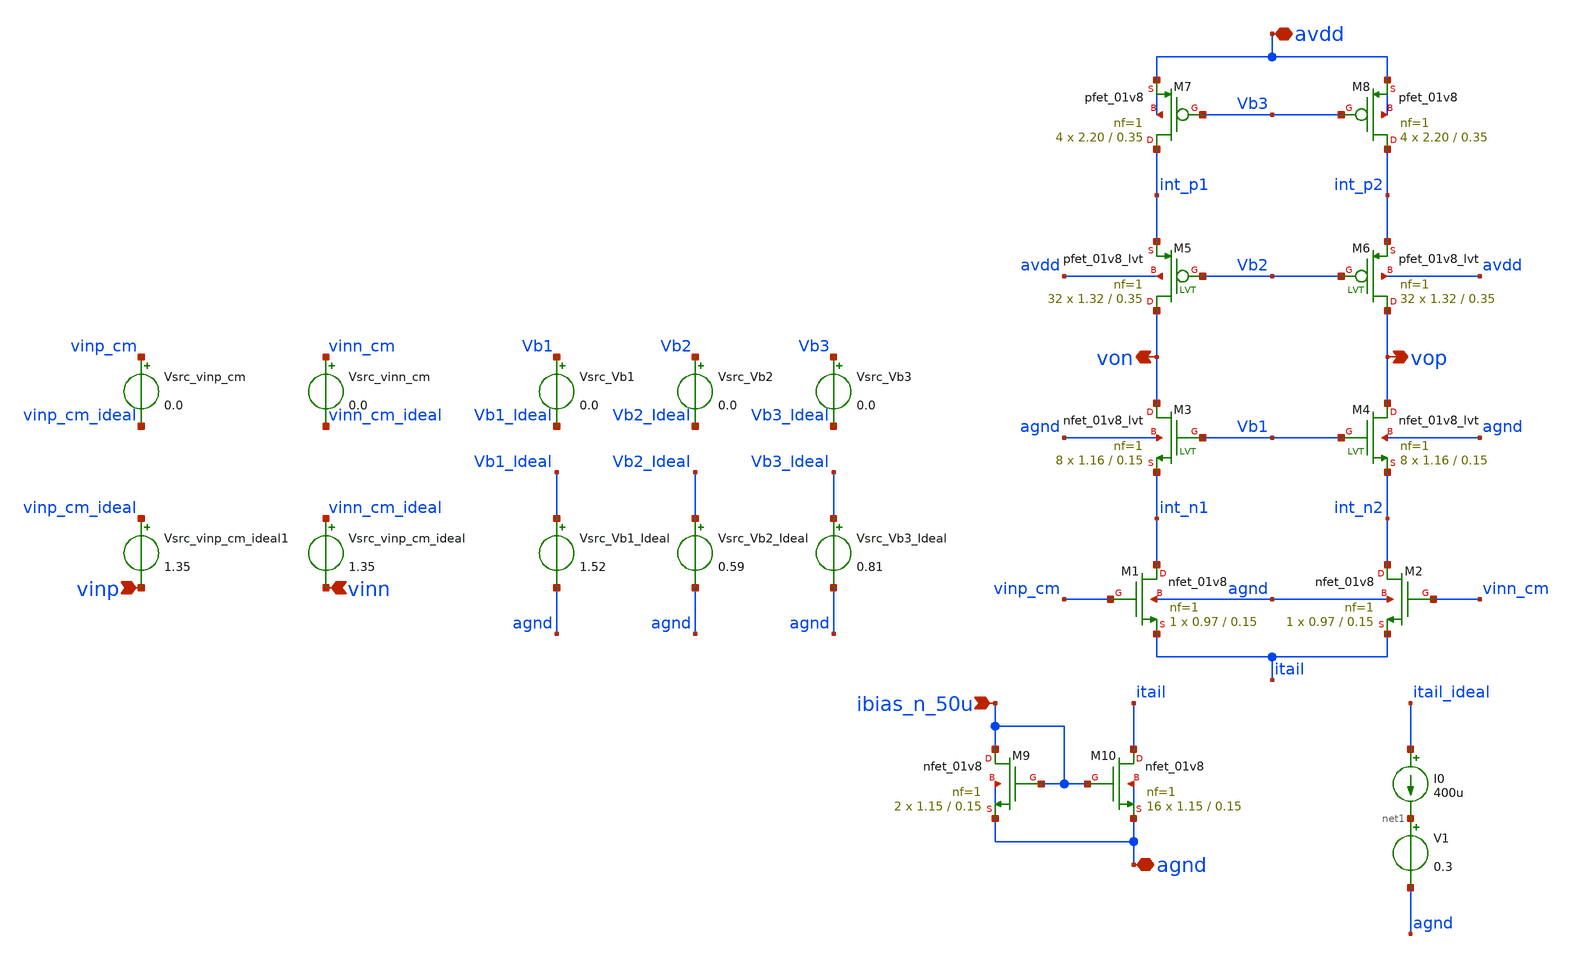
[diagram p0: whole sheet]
** sch_path: AMP/Final_Cascode_Mixed.sch
**.subckt Final_Cascode_Mixed avdd vinp vop agnd vinn von ibias_n_50u
*.iopin avdd
*.ipin vinp
*.opin vop
*.iopin agnd
*.ipin vinn
*.opin von
*.ipin ibias_n_50u
Vsrc_Vb3_Ideal Vb3_Ideal agnd 0.81
Vsrc_Vb2_Ideal Vb2_Ideal agnd 0.59
Vsrc_Vb1_Ideal Vb1_Ideal agnd 1.52
Vsrc_Vb3 Vb3 Vb3_Ideal 0.0
Vsrc_Vb2 Vb2 Vb2_Ideal 0.0
Vsrc_Vb1 Vb1 Vb1_Ideal 0.0
Vsrc_vinp_cm_ideal1 vinp_cm_ideal vinp 1.35
Vsrc_vinp_cm_ideal vinn_cm_ideal vinn 1.35
Vsrc_vinn_cm vinn_cm vinn_cm_ideal 0.0
Vsrc_vinp_cm vinp_cm vinp_cm_ideal 0.0
XM1 int_n1 vinp_cm itail agnd sky130_fd_pr__nfet_01v8 L=0.15 W=0.97 nf=1 ad='int((nf+1)/2) * W/nf * 0.29'
+ as='int((nf+2)/2) * W/nf * 0.29' pd='2*int((nf+1)/2) * (W/nf + 0.29)' ps='2*int((nf+2)/2) * (W/nf + 0.29)'
+ nrd='0.29 / W' nrs='0.29 / W' sa=0 sb=0 sd=0 mult=1 m=1
XM2 int_n2 vinn_cm itail agnd sky130_fd_pr__nfet_01v8 L=0.15 W=0.97 nf=1 ad='int((nf+1)/2) * W/nf * 0.29'
+ as='int((nf+2)/2) * W/nf * 0.29' pd='2*int((nf+1)/2) * (W/nf + 0.29)' ps='2*int((nf+2)/2) * (W/nf + 0.29)'
+ nrd='0.29 / W' nrs='0.29 / W' sa=0 sb=0 sd=0 mult=1 m=1
XM7 int_p1 Vb3 avdd avdd sky130_fd_pr__pfet_01v8 L=0.35 W=2.20 nf=1 ad='int((nf+1)/2) * W/nf * 0.29'
+ as='int((nf+2)/2) * W/nf * 0.29' pd='2*int((nf+1)/2) * (W/nf + 0.29)' ps='2*int((nf+2)/2) * (W/nf + 0.29)'
+ nrd='0.29 / W' nrs='0.29 / W' sa=0 sb=0 sd=0 mult=4 m=4
XM8 int_p2 Vb3 avdd avdd sky130_fd_pr__pfet_01v8 L=0.35 W=2.20 nf=1 ad='int((nf+1)/2) * W/nf * 0.29'
+ as='int((nf+2)/2) * W/nf * 0.29' pd='2*int((nf+1)/2) * (W/nf + 0.29)' ps='2*int((nf+2)/2) * (W/nf + 0.29)'
+ nrd='0.29 / W' nrs='0.29 / W' sa=0 sb=0 sd=0 mult=4 m=4
XM9 ibias_n_50u ibias_n_50u agnd agnd sky130_fd_pr__nfet_01v8 L=0.15 W=1.15 nf=1 ad='int((nf+1)/2) * W/nf * 0.29'
+ as='int((nf+2)/2) * W/nf * 0.29' pd='2*int((nf+1)/2) * (W/nf + 0.29)' ps='2*int((nf+2)/2) * (W/nf + 0.29)'
+ nrd='0.29 / W' nrs='0.29 / W' sa=0 sb=0 sd=0 mult=2 m=2
XM10 itail ibias_n_50u agnd agnd sky130_fd_pr__nfet_01v8 L=0.15 W=1.15 nf=1 ad='int((nf+1)/2) * W/nf * 0.29'
+ as='int((nf+2)/2) * W/nf * 0.29' pd='2*int((nf+1)/2) * (W/nf + 0.29)' ps='2*int((nf+2)/2) * (W/nf + 0.29)'
+ nrd='0.29 / W' nrs='0.29 / W' sa=0 sb=0 sd=0 mult=16 m=16
XM3 von Vb1 int_n1 agnd sky130_fd_pr__nfet_01v8_lvt L=0.15 W=1.16 nf=1 ad='int((nf+1)/2) * W/nf * 0.29'
+ as='int((nf+2)/2) * W/nf * 0.29' pd='2*int((nf+1)/2) * (W/nf + 0.29)' ps='2*int((nf+2)/2) * (W/nf + 0.29)'
+ nrd='0.29 / W' nrs='0.29 / W' sa=0 sb=0 sd=0 mult=8 m=8
XM4 vop Vb1 int_n2 agnd sky130_fd_pr__nfet_01v8_lvt L=0.15 W=1.16 nf=1 ad='int((nf+1)/2) * W/nf * 0.29'
+ as='int((nf+2)/2) * W/nf * 0.29' pd='2*int((nf+1)/2) * (W/nf + 0.29)' ps='2*int((nf+2)/2) * (W/nf + 0.29)'
+ nrd='0.29 / W' nrs='0.29 / W' sa=0 sb=0 sd=0 mult=8 m=8
XM5 von Vb2 int_p1 avdd sky130_fd_pr__pfet_01v8_lvt L=0.35 W=1.32 nf=1 ad='int((nf+1)/2) * W/nf * 0.29'
+ as='int((nf+2)/2) * W/nf * 0.29' pd='2*int((nf+1)/2) * (W/nf + 0.29)' ps='2*int((nf+2)/2) * (W/nf + 0.29)'
+ nrd='0.29 / W' nrs='0.29 / W' sa=0 sb=0 sd=0 mult=32 m=32
XM6 vop Vb2 int_p2 avdd sky130_fd_pr__pfet_01v8_lvt L=0.35 W=1.32 nf=1 ad='int((nf+1)/2) * W/nf * 0.29'
+ as='int((nf+2)/2) * W/nf * 0.29' pd='2*int((nf+1)/2) * (W/nf + 0.29)' ps='2*int((nf+2)/2) * (W/nf + 0.29)'
+ nrd='0.29 / W' nrs='0.29 / W' sa=0 sb=0 sd=0 mult=32 m=32
I0 itail_ideal net1 400u
V1 net1 agnd 0.3
**.ends
.end
